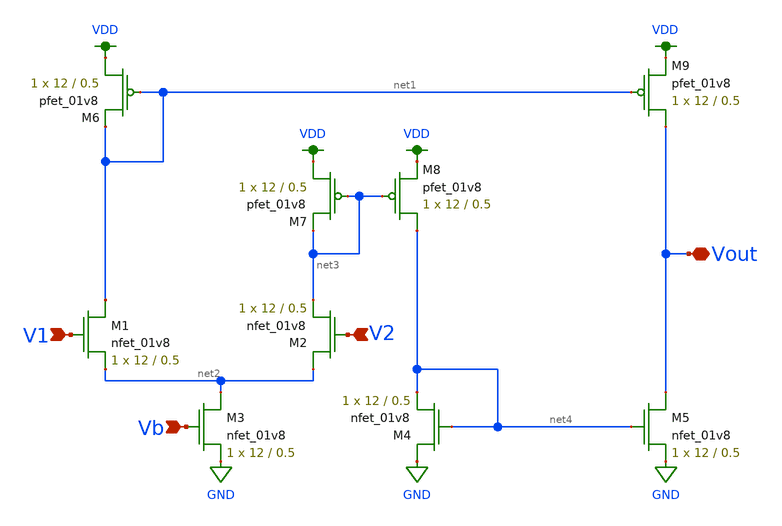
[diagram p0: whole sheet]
** sch_path: schematic/archive/nmos_current_mirror_diff_amp.sch
**.subckt nmos_current_mirror_diff_amp V1 V2 Vb Vout
*.ipin V1
*.ipin V2
*.ipin Vb
*.iopin Vout
XM1 net1 V1 net2 GND sky130_fd_pr__nfet_01v8 L=0.5 W=12 nf=1 ad='int((nf+1)/2) * W/nf * 0.29' as='int((nf+2)/2) * W/nf * 0.29'
+ pd='2*int((nf+1)/2) * (W/nf + 0.29)' ps='2*int((nf+2)/2) * (W/nf + 0.29)' nrd='0.29 / W' nrs='0.29 / W'
+ sa=0 sb=0 sd=0 mult=1 m=1
XM2 net2 V2 net3 GND sky130_fd_pr__nfet_01v8 L=0.5 W=12 nf=1 ad='int((nf+1)/2) * W/nf * 0.29' as='int((nf+2)/2) * W/nf * 0.29'
+ pd='2*int((nf+1)/2) * (W/nf + 0.29)' ps='2*int((nf+2)/2) * (W/nf + 0.29)' nrd='0.29 / W' nrs='0.29 / W'
+ sa=0 sb=0 sd=0 mult=1 m=1
XM3 net2 Vb GND GND sky130_fd_pr__nfet_01v8 L=0.5 W=12 nf=1 ad='int((nf+1)/2) * W/nf * 0.29' as='int((nf+2)/2) * W/nf * 0.29'
+ pd='2*int((nf+1)/2) * (W/nf + 0.29)' ps='2*int((nf+2)/2) * (W/nf + 0.29)' nrd='0.29 / W' nrs='0.29 / W'
+ sa=0 sb=0 sd=0 mult=1 m=1
XM4 GND net4 net4 GND sky130_fd_pr__nfet_01v8 L=0.5 W=12 nf=1 ad='int((nf+1)/2) * W/nf * 0.29' as='int((nf+2)/2) * W/nf * 0.29'
+ pd='2*int((nf+1)/2) * (W/nf + 0.29)' ps='2*int((nf+2)/2) * (W/nf + 0.29)' nrd='0.29 / W' nrs='0.29 / W'
+ sa=0 sb=0 sd=0 mult=1 m=1
XM5 Vout net4 GND GND sky130_fd_pr__nfet_01v8 L=0.5 W=12 nf=1 ad='int((nf+1)/2) * W/nf * 0.29' as='int((nf+2)/2) * W/nf * 0.29'
+ pd='2*int((nf+1)/2) * (W/nf + 0.29)' ps='2*int((nf+2)/2) * (W/nf + 0.29)' nrd='0.29 / W' nrs='0.29 / W'
+ sa=0 sb=0 sd=0 mult=1 m=1
XM6 VDD net1 net1 VDD sky130_fd_pr__pfet_01v8 L=0.5 W=12 nf=1 ad='int((nf+1)/2) * W/nf * 0.29' as='int((nf+2)/2) * W/nf * 0.29'
+ pd='2*int((nf+1)/2) * (W/nf + 0.29)' ps='2*int((nf+2)/2) * (W/nf + 0.29)' nrd='0.29 / W' nrs='0.29 / W'
+ sa=0 sb=0 sd=0 mult=1 m=1
XM7 VDD net3 net3 VDD sky130_fd_pr__pfet_01v8 L=0.5 W=12 nf=1 ad='int((nf+1)/2) * W/nf * 0.29' as='int((nf+2)/2) * W/nf * 0.29'
+ pd='2*int((nf+1)/2) * (W/nf + 0.29)' ps='2*int((nf+2)/2) * (W/nf + 0.29)' nrd='0.29 / W' nrs='0.29 / W'
+ sa=0 sb=0 sd=0 mult=1 m=1
XM8 net4 net3 VDD VDD sky130_fd_pr__pfet_01v8 L=0.5 W=12 nf=1 ad='int((nf+1)/2) * W/nf * 0.29' as='int((nf+2)/2) * W/nf * 0.29'
+ pd='2*int((nf+1)/2) * (W/nf + 0.29)' ps='2*int((nf+2)/2) * (W/nf + 0.29)' nrd='0.29 / W' nrs='0.29 / W'
+ sa=0 sb=0 sd=0 mult=1 m=1
XM9 Vout net1 VDD VDD sky130_fd_pr__pfet_01v8 L=0.5 W=12 nf=1 ad='int((nf+1)/2) * W/nf * 0.29' as='int((nf+2)/2) * W/nf * 0.29'
+ pd='2*int((nf+1)/2) * (W/nf + 0.29)' ps='2*int((nf+2)/2) * (W/nf + 0.29)' nrd='0.29 / W' nrs='0.29 / W'
+ sa=0 sb=0 sd=0 mult=1 m=1
**.ends
.GLOBAL GND
.GLOBAL VDD
.end
